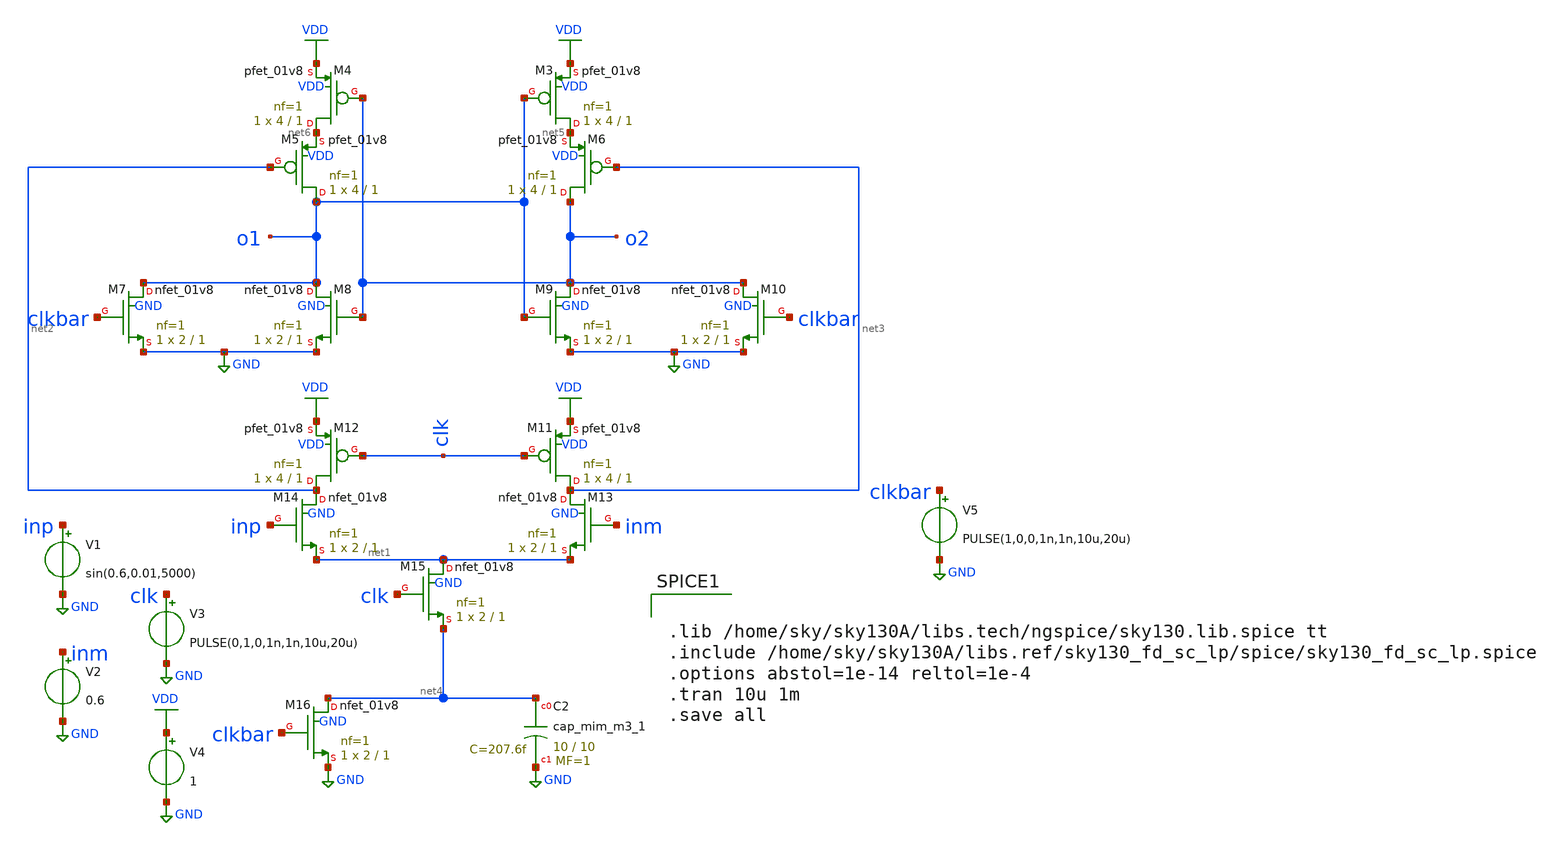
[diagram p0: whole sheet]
** sch_path: xschem/comparator/doubletaillatch_tb.sch
**.subckt doubletaillatch_tb
V1 inp GND sin(0.6,0.01,5000)
XM3 net5 o1 VDD VDD sky130_fd_pr__pfet_01v8 L=1 W=4 nf=1 ad='int((nf+1)/2) * W/nf * 0.29' as='int((nf+2)/2) * W/nf * 0.29'
+ pd='2*int((nf+1)/2) * (W/nf + 0.29)' ps='2*int((nf+2)/2) * (W/nf + 0.29)' nrd='0.29 / W' nrs='0.29 / W'
+ sa=0 sb=0 sd=0 mult=1 m=1
XM4 net6 o2 VDD VDD sky130_fd_pr__pfet_01v8 L=1 W=4 nf=1 ad='int((nf+1)/2) * W/nf * 0.29' as='int((nf+2)/2) * W/nf * 0.29'
+ pd='2*int((nf+1)/2) * (W/nf + 0.29)' ps='2*int((nf+2)/2) * (W/nf + 0.29)' nrd='0.29 / W' nrs='0.29 / W'
+ sa=0 sb=0 sd=0 mult=1 m=1
XM5 o1 net2 net6 VDD sky130_fd_pr__pfet_01v8 L=1 W=4 nf=1 ad='int((nf+1)/2) * W/nf * 0.29' as='int((nf+2)/2) * W/nf * 0.29'
+ pd='2*int((nf+1)/2) * (W/nf + 0.29)' ps='2*int((nf+2)/2) * (W/nf + 0.29)' nrd='0.29 / W' nrs='0.29 / W'
+ sa=0 sb=0 sd=0 mult=1 m=1
XM6 o2 net3 net5 VDD sky130_fd_pr__pfet_01v8 L=1 W=4 nf=1 ad='int((nf+1)/2) * W/nf * 0.29' as='int((nf+2)/2) * W/nf * 0.29'
+ pd='2*int((nf+1)/2) * (W/nf + 0.29)' ps='2*int((nf+2)/2) * (W/nf + 0.29)' nrd='0.29 / W' nrs='0.29 / W'
+ sa=0 sb=0 sd=0 mult=1 m=1
XM7 o1 clkbar GND GND sky130_fd_pr__nfet_01v8 L=1 W=2 nf=1 ad='int((nf+1)/2) * W/nf * 0.29' as='int((nf+2)/2) * W/nf * 0.29'
+ pd='2*int((nf+1)/2) * (W/nf + 0.29)' ps='2*int((nf+2)/2) * (W/nf + 0.29)' nrd='0.29 / W' nrs='0.29 / W'
+ sa=0 sb=0 sd=0 mult=1 m=1
XM8 o1 o2 GND GND sky130_fd_pr__nfet_01v8 L=1 W=2 nf=1 ad='int((nf+1)/2) * W/nf * 0.29' as='int((nf+2)/2) * W/nf * 0.29'
+ pd='2*int((nf+1)/2) * (W/nf + 0.29)' ps='2*int((nf+2)/2) * (W/nf + 0.29)' nrd='0.29 / W' nrs='0.29 / W'
+ sa=0 sb=0 sd=0 mult=1 m=1
XM9 o2 o1 GND GND sky130_fd_pr__nfet_01v8 L=1 W=2 nf=1 ad='int((nf+1)/2) * W/nf * 0.29' as='int((nf+2)/2) * W/nf * 0.29'
+ pd='2*int((nf+1)/2) * (W/nf + 0.29)' ps='2*int((nf+2)/2) * (W/nf + 0.29)' nrd='0.29 / W' nrs='0.29 / W'
+ sa=0 sb=0 sd=0 mult=1 m=1
XM10 o2 clkbar GND GND sky130_fd_pr__nfet_01v8 L=1 W=2 nf=1 ad='int((nf+1)/2) * W/nf * 0.29' as='int((nf+2)/2) * W/nf * 0.29'
+ pd='2*int((nf+1)/2) * (W/nf + 0.29)' ps='2*int((nf+2)/2) * (W/nf + 0.29)' nrd='0.29 / W' nrs='0.29 / W'
+ sa=0 sb=0 sd=0 mult=1 m=1
XM11 net3 clk VDD VDD sky130_fd_pr__pfet_01v8 L=1 W=4 nf=1 ad='int((nf+1)/2) * W/nf * 0.29' as='int((nf+2)/2) * W/nf * 0.29'
+ pd='2*int((nf+1)/2) * (W/nf + 0.29)' ps='2*int((nf+2)/2) * (W/nf + 0.29)' nrd='0.29 / W' nrs='0.29 / W'
+ sa=0 sb=0 sd=0 mult=1 m=1
XM12 net2 clk VDD VDD sky130_fd_pr__pfet_01v8 L=1 W=4 nf=1 ad='int((nf+1)/2) * W/nf * 0.29' as='int((nf+2)/2) * W/nf * 0.29'
+ pd='2*int((nf+1)/2) * (W/nf + 0.29)' ps='2*int((nf+2)/2) * (W/nf + 0.29)' nrd='0.29 / W' nrs='0.29 / W'
+ sa=0 sb=0 sd=0 mult=1 m=1
XM13 net3 inm net1 GND sky130_fd_pr__nfet_01v8 L=1 W=2 nf=1 ad='int((nf+1)/2) * W/nf * 0.29' as='int((nf+2)/2) * W/nf * 0.29'
+ pd='2*int((nf+1)/2) * (W/nf + 0.29)' ps='2*int((nf+2)/2) * (W/nf + 0.29)' nrd='0.29 / W' nrs='0.29 / W'
+ sa=0 sb=0 sd=0 mult=1 m=1
XM14 net2 inp net1 GND sky130_fd_pr__nfet_01v8 L=1 W=2 nf=1 ad='int((nf+1)/2) * W/nf * 0.29' as='int((nf+2)/2) * W/nf * 0.29'
+ pd='2*int((nf+1)/2) * (W/nf + 0.29)' ps='2*int((nf+2)/2) * (W/nf + 0.29)' nrd='0.29 / W' nrs='0.29 / W'
+ sa=0 sb=0 sd=0 mult=1 m=1
XM15 net1 clk net4 GND sky130_fd_pr__nfet_01v8 L=1 W=2 nf=1 ad='int((nf+1)/2) * W/nf * 0.29' as='int((nf+2)/2) * W/nf * 0.29'
+ pd='2*int((nf+1)/2) * (W/nf + 0.29)' ps='2*int((nf+2)/2) * (W/nf + 0.29)' nrd='0.29 / W' nrs='0.29 / W'
+ sa=0 sb=0 sd=0 mult=1 m=1
XM16 net4 clkbar GND GND sky130_fd_pr__nfet_01v8 L=1 W=2 nf=1 ad='int((nf+1)/2) * W/nf * 0.29' as='int((nf+2)/2) * W/nf * 0.29'
+ pd='2*int((nf+1)/2) * (W/nf + 0.29)' ps='2*int((nf+2)/2) * (W/nf + 0.29)' nrd='0.29 / W' nrs='0.29 / W'
+ sa=0 sb=0 sd=0 mult=1 m=1
XC2 net4 GND sky130_fd_pr__cap_mim_m3_1 W=10 L=10 MF=1 m=1
V2 inm GND 0.6
V3 clk GND PULSE(0,1,0,1n,1n,10u,20u)
V4 VDD GND 1
V5 clkbar GND PULSE(1,0,0,1n,1n,10u,20u)
**** begin user architecture code


.lib /home/sky/sky130A/libs.tech/ngspice/sky130.lib.spice tt
.include /home/sky/sky130A/libs.ref/sky130_fd_sc_lp/spice/sky130_fd_sc_lp.spice
.options abstol=1e-14 reltol=1e-4
.tran 10u 1m
.save all


**** end user architecture code
**.ends
.GLOBAL VDD
.GLOBAL GND
.end
